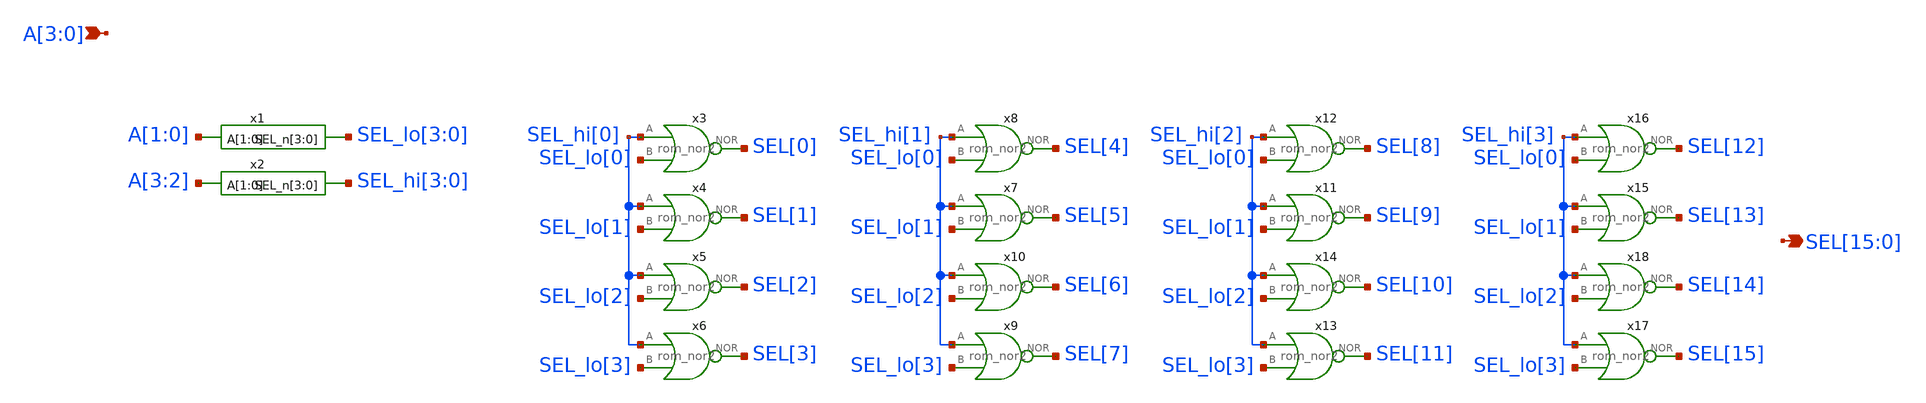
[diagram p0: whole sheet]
** sch_path: blocks/rom/rom_dec_4b.sch
**.subckt rom_dec_4b
*+ SEL[15],SEL[14],SEL[13],SEL[12],SEL[11],SEL[10],SEL[9],SEL[8],SEL[7],SEL[6],SEL[5],SEL[4],SEL[3],SEL[2],SEL[1],SEL[0] A[3],A[2],A[1],A[0]
*.opin
*+ SEL[15],SEL[14],SEL[13],SEL[12],SEL[11],SEL[10],SEL[9],SEL[8],SEL[7],SEL[6],SEL[5],SEL[4],SEL[3],SEL[2],SEL[1],SEL[0]
*.ipin A[3],A[2],A[1],A[0]
x1 A[1] A[0] SEL_lo[3] SEL_lo[2] SEL_lo[1] SEL_lo[0] rom_dec_2b
x2 A[3] A[2] SEL_hi[3] SEL_hi[2] SEL_hi[1] SEL_hi[0] rom_dec_2b
x4 SEL_hi[0] SEL_lo[1] SEL[1] rom_nor2
x3 SEL_hi[0] SEL_lo[0] SEL[0] rom_nor2
x6 SEL_hi[0] SEL_lo[3] SEL[3] rom_nor2
x5 SEL_hi[0] SEL_lo[2] SEL[2] rom_nor2
x7 SEL_hi[1] SEL_lo[1] SEL[5] rom_nor2
x8 SEL_hi[1] SEL_lo[0] SEL[4] rom_nor2
x9 SEL_hi[1] SEL_lo[3] SEL[7] rom_nor2
x10 SEL_hi[1] SEL_lo[2] SEL[6] rom_nor2
x11 SEL_hi[2] SEL_lo[1] SEL[9] rom_nor2
x12 SEL_hi[2] SEL_lo[0] SEL[8] rom_nor2
x13 SEL_hi[2] SEL_lo[3] SEL[11] rom_nor2
x14 SEL_hi[2] SEL_lo[2] SEL[10] rom_nor2
x15 SEL_hi[3] SEL_lo[1] SEL[13] rom_nor2
x16 SEL_hi[3] SEL_lo[0] SEL[12] rom_nor2
x17 SEL_hi[3] SEL_lo[3] SEL[15] rom_nor2
x18 SEL_hi[3] SEL_lo[2] SEL[14] rom_nor2
**.ends
.end
